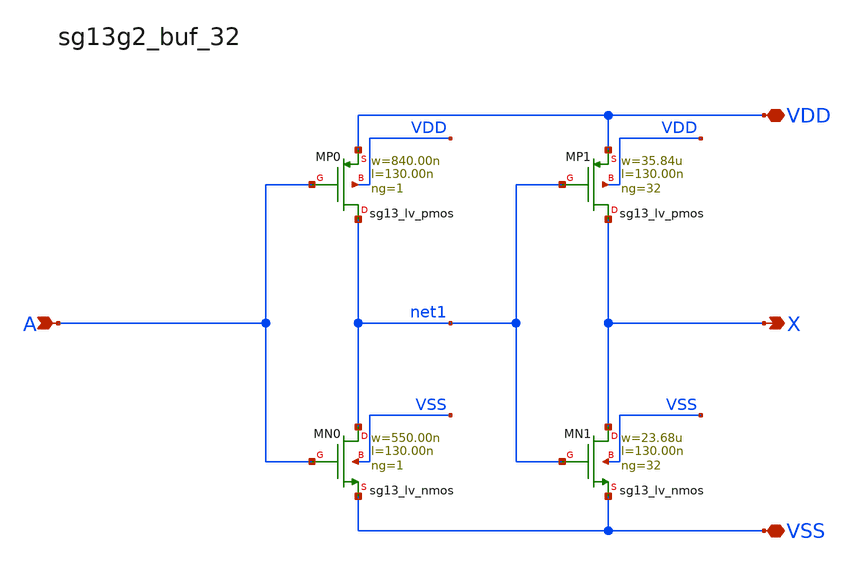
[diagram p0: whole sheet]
** sch_path: outputs/sg13g2_cells/cells/sg13g2_buf_32/sg13g2_buf_32.sch
* Copyright 2024  IHP PDK Authors
* Copyright 2023  IHP PDK Authors
**.subckt sg13g2_buf_32 X A VDD VSS
*.opin X
*.ipin A
*.iopin VDD
*.iopin VSS
XMN0 net1 A VSS VSS sg13_lv_nmos w=550.00n l=130.00n ng=1
XMN1 X net1 VSS VSS sg13_lv_nmos w=23.68u l=130.00n ng=32
XMP1 X net1 VDD VDD sg13_lv_pmos w=35.84u l=130.00n ng=32
XMP0 net1 A VDD VDD sg13_lv_pmos w=840.00n l=130.00n ng=1
**.ends
.end
